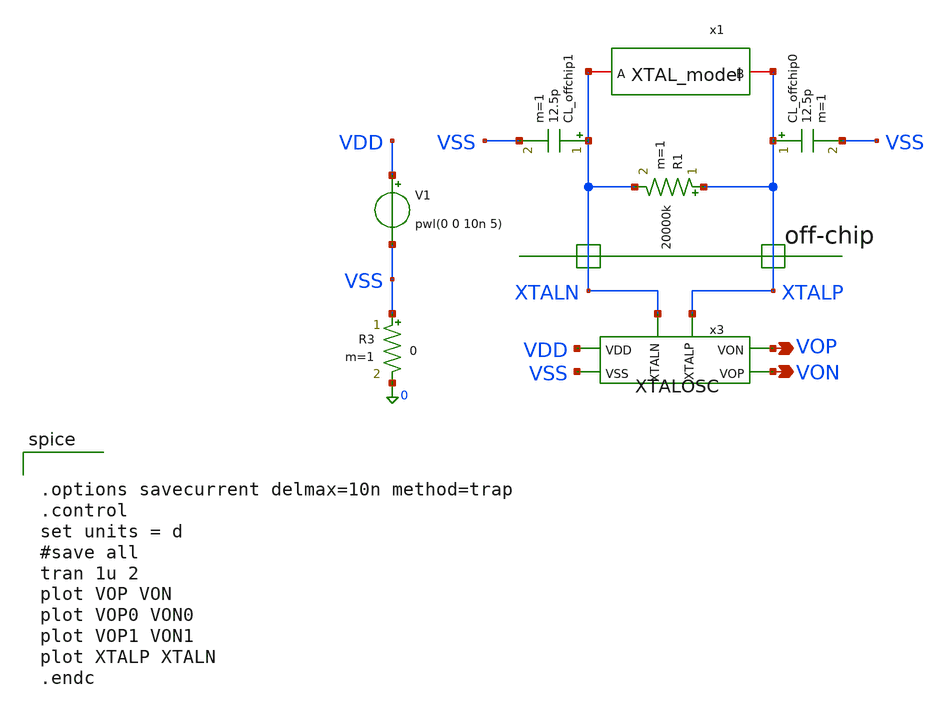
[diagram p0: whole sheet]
** sch_path: member_project/JJY_Receiver/Masahiro/jjy_recv/XTALOSC/XTALOSC_sim_v2.sch
**.subckt XTALOSC_sim_v2 VON VOP
*.opin VON
*.opin VOP
R1 XTALP XTALN 20000k m=1
CL_offchip0 XTALP VSS 12.5p m=1
CL_offchip1 XTALN VSS 12.5p m=1
V1 VDD VSS pwl(0 0 10n 5)
R3 VSS 0 0 m=1
x1 XTALN XTALP XTAL_model
x3 VDD VSS VOP XTALN XTALP VON XTALOSC
**** begin user architecture code
 .include $::LIB/ip62_models


.options savecurrent delmax=10n method=trap
.control
set units = d
#save all
tran 1u 2
plot VOP VON
plot VOP0 VON0
plot VOP1 VON1
plot XTALP XTALN
.endc


**** end user architecture code
**.ends
.end
